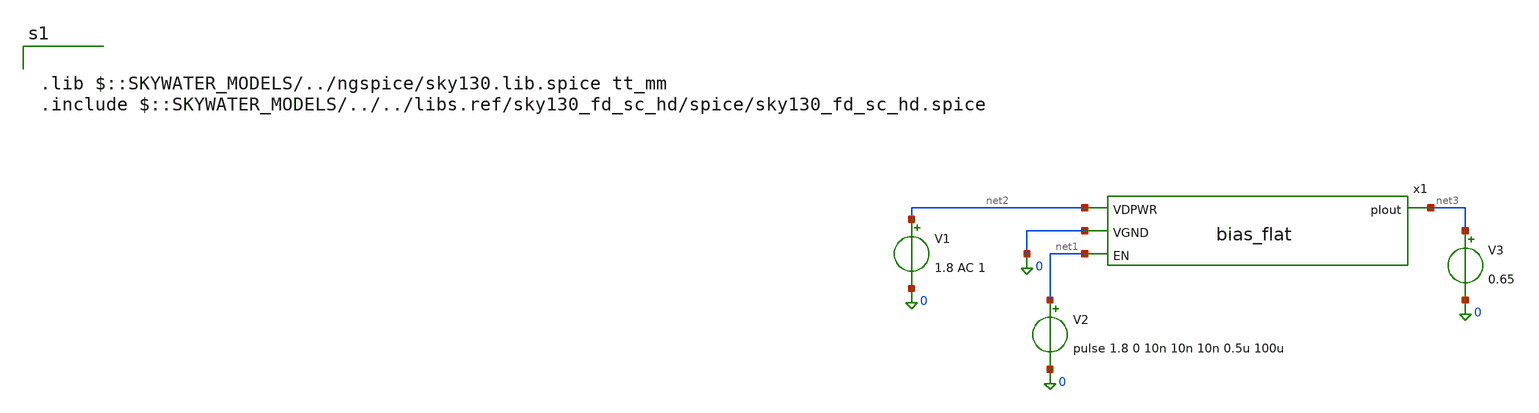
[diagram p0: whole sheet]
** sch_path: xschem/tb_bias.sch
**.subckt tb_bias
V1 net2 0 1.8 AC 1
V2 net1 0 pulse 1.8 0 10n 10n 10n 0.5u 100u
x1 net2 net3 0 net1 bias_flat
V3 net3 0 0.65
.save i(v3)
**** begin user architecture code


*.options savecurrents
*.save all
.control
let run = 0
dowhile run < 128
  dc TEMP -40 125 15 v1 1.6 2 0.2
*  plot i(v3)
  write reference.raw
  set appendwrite
  let run = run+1
  reset
end
.endc




.lib $::SKYWATER_MODELS/../ngspice/sky130.lib.spice tt_mm
.include $::SKYWATER_MODELS/../../libs.ref/sky130_fd_sc_hd/spice/sky130_fd_sc_hd.spice


**** end user architecture code
**.ends

* expanding   symbol:  /foss/designs/ttsky26c-analog-park/xschem/bias_flat.sym # of pins=4
** sym_path: xschem/bias.sym
.include /foss/designs/ttsky26c-analog-park/mag/pex/pex_bias.spice
.end
